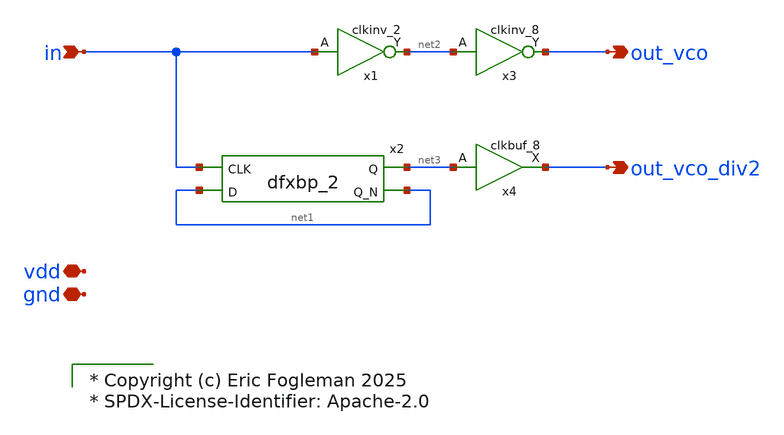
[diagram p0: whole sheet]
** sch_path: xschem/ejf_pll96_outbuf.sch

* Copyright (c) Eric Fogleman 2025
* SPDX-License-Identifier: Apache-2.0

**.subckt ejf_pll96_outbuf in out_vco_div2 vdd out_vco gnd
*.ipin in
*.opin out_vco_div2
*.iopin vdd
*.opin out_vco
*.iopin gnd
x1 in gnd gnd vdd vdd net2 sky130_fd_sc_ls__clkinv_2
x2 in net1 gnd gnd vdd vdd net3 net1 sky130_fd_sc_ls__dfxbp_2
x3 net2 gnd gnd vdd vdd out_vco sky130_fd_sc_ls__clkinv_8
x4 net3 gnd gnd vdd vdd out_vco_div2 sky130_fd_sc_ls__clkbuf_8
**.ends
.end
